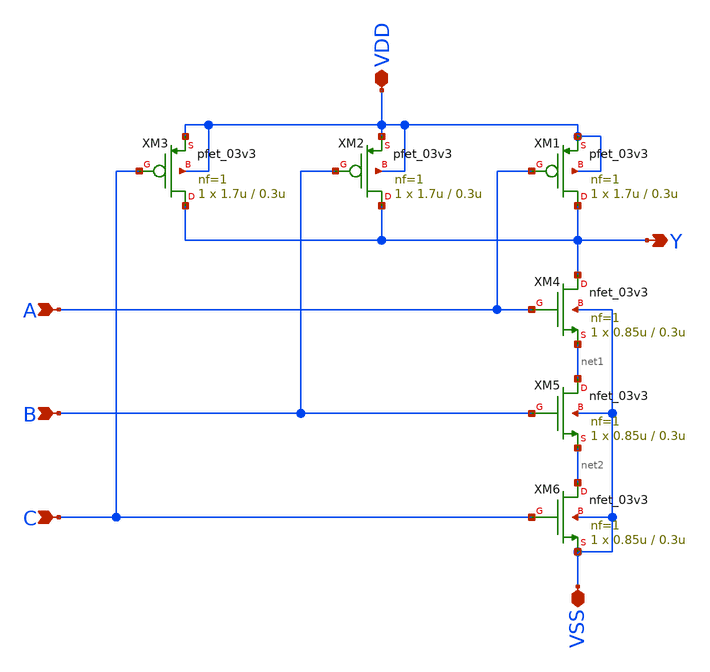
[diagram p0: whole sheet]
** sch_path: designs/libs/tb_NAND3/gf180mcu_osu_sc_gp9t3v3__nand3_1.sch
**.subckt gf180mcu_osu_sc_gp9t3v3__nand3_1 A B C Y VDD VSS
*.ipin A
*.ipin B
*.ipin C
*.opin Y
*.iopin VDD
*.iopin VSS
XM1 Y A VDD VDD pfet_03v3 L=0.3u W=1.7u nf=1 ad='int((nf+1)/2) * W/nf * 0.18u' as='int((nf+2)/2) * W/nf * 0.18u'
+ pd='2*int((nf+1)/2) * (W/nf + 0.18u)' ps='2*int((nf+2)/2) * (W/nf + 0.18u)' nrd='0.18u / W' nrs='0.18u / W'
+ sa=0 sb=0 sd=0 m=1
XM2 Y B VDD VDD pfet_03v3 L=0.3u W=1.7u nf=1 ad='int((nf+1)/2) * W/nf * 0.18u' as='int((nf+2)/2) * W/nf * 0.18u'
+ pd='2*int((nf+1)/2) * (W/nf + 0.18u)' ps='2*int((nf+2)/2) * (W/nf + 0.18u)' nrd='0.18u / W' nrs='0.18u / W'
+ sa=0 sb=0 sd=0 m=1
XM3 Y C VDD VDD pfet_03v3 L=0.3u W=1.7u nf=1 ad='int((nf+1)/2) * W/nf * 0.18u' as='int((nf+2)/2) * W/nf * 0.18u'
+ pd='2*int((nf+1)/2) * (W/nf + 0.18u)' ps='2*int((nf+2)/2) * (W/nf + 0.18u)' nrd='0.18u / W' nrs='0.18u / W'
+ sa=0 sb=0 sd=0 m=1
XM4 Y A net1 VSS nfet_03v3 L=0.3u W=0.85u nf=1 ad='int((nf+1)/2) * W/nf * 0.18u' as='int((nf+2)/2) * W/nf * 0.18u'
+ pd='2*int((nf+1)/2) * (W/nf + 0.18u)' ps='2*int((nf+2)/2) * (W/nf + 0.18u)' nrd='0.18u / W' nrs='0.18u / W'
+ sa=0 sb=0 sd=0 m=1
XM5 net1 B net2 VSS nfet_03v3 L=0.3u W=0.85u nf=1 ad='int((nf+1)/2) * W/nf * 0.18u' as='int((nf+2)/2) * W/nf * 0.18u'
+ pd='2*int((nf+1)/2) * (W/nf + 0.18u)' ps='2*int((nf+2)/2) * (W/nf + 0.18u)' nrd='0.18u / W' nrs='0.18u / W'
+ sa=0 sb=0 sd=0 m=1
XM6 net2 C VSS VSS nfet_03v3 L=0.3u W=0.85u nf=1 ad='int((nf+1)/2) * W/nf * 0.18u' as='int((nf+2)/2) * W/nf * 0.18u'
+ pd='2*int((nf+1)/2) * (W/nf + 0.18u)' ps='2*int((nf+2)/2) * (W/nf + 0.18u)' nrd='0.18u / W' nrs='0.18u / W'
+ sa=0 sb=0 sd=0 m=1
**.ends
.end
